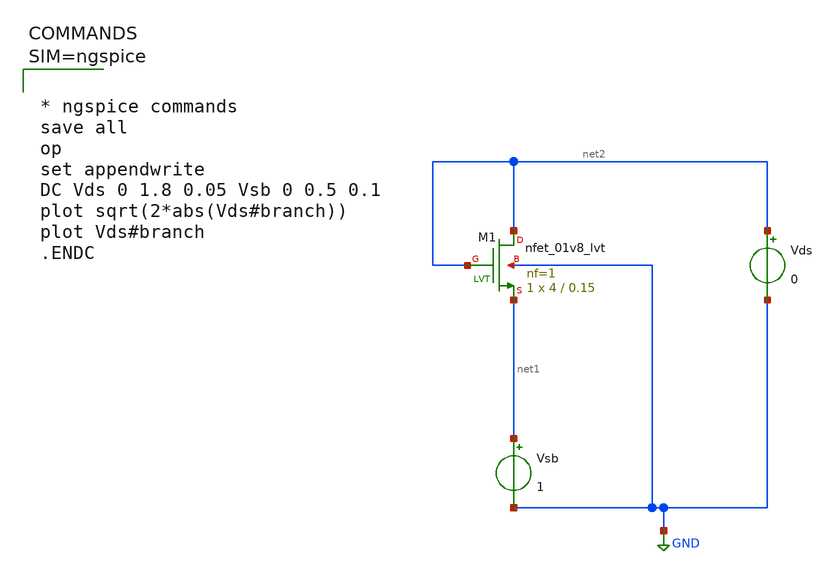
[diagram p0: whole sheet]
** sch_path: work/xschem/untitled-3.sch
**.subckt untitled-3
XM1 net2 net2 net1 GND sky130_fd_pr__nfet_01v8_lvt L=0.15 W=4 nf=1 ad='int((1 + 1)/2) * 4 / 1 * 0.29'
+ as='int((1 + 2)/2) * 4 / 1 * 0.29' pd='2*int((1 + 1)/2) * (4 / 1 + 0.29)' ps='2*int((1 + 2)/2) * (4 / 1 + 0.29)'
+ nrd='0.29 / 4 ' nrs='0.29 / 4 ' sa=0 sb=0 sd=0 mult=1 m=1
Vsb net1 GND 1
Vds net2 GND 0
**** begin user architecture code



* ngspice commands
save all
op
set appendwrite
DC Vds 0 1.8 0.05 Vsb 0 0.5 0.1
plot sqrt(2*abs(Vds#branch))
plot Vds#branch
.ENDC



**** end user architecture code
**.ends
.GLOBAL GND
.end
